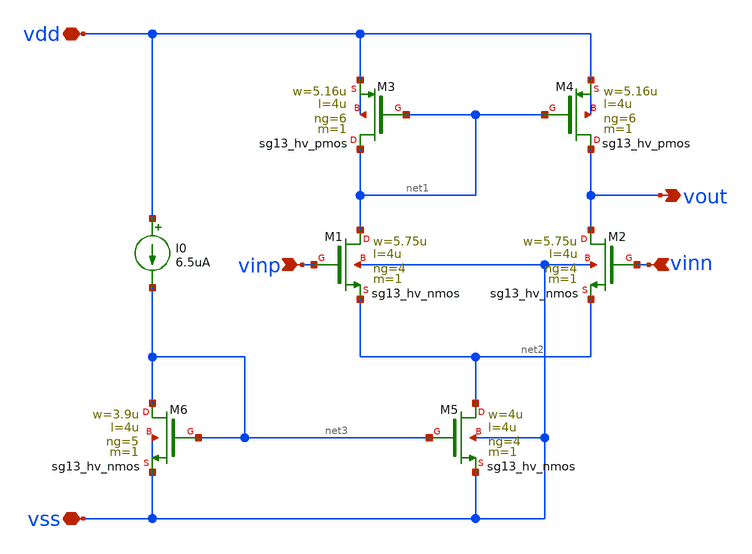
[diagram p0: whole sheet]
** sch_path: real_circuit/sandbox/simple_OTA.sch
**.subckt simple_OTA vout vdd vss vinp vinn
*.opin vout
*.iopin vdd
*.iopin vss
*.ipin vinp
*.ipin vinn
XM1 net1 vinp net2 vss sg13_hv_nmos w=5.75u l=4u ng=4 m=1 mm_ok=1
XM2 vout vinn net2 vss sg13_hv_nmos w=5.75u l=4u ng=4 m=1 mm_ok=1
XM3 net1 net1 vdd vdd sg13_hv_pmos w=5.16u l=4u ng=6 m=1 mm_ok=1
XM4 vout net1 vdd vdd sg13_hv_pmos w=5.16u l=4u ng=6 m=1 mm_ok=1
XM5 net2 net3 vss vss sg13_hv_nmos w=4u l=4u ng=4 m=1 mm_ok=1
XM6 net3 net3 vss vss sg13_hv_nmos w=3.9u l=4u ng=5 m=1 mm_ok=1
I0 vdd net3 6.5uA
**.ends
.end
